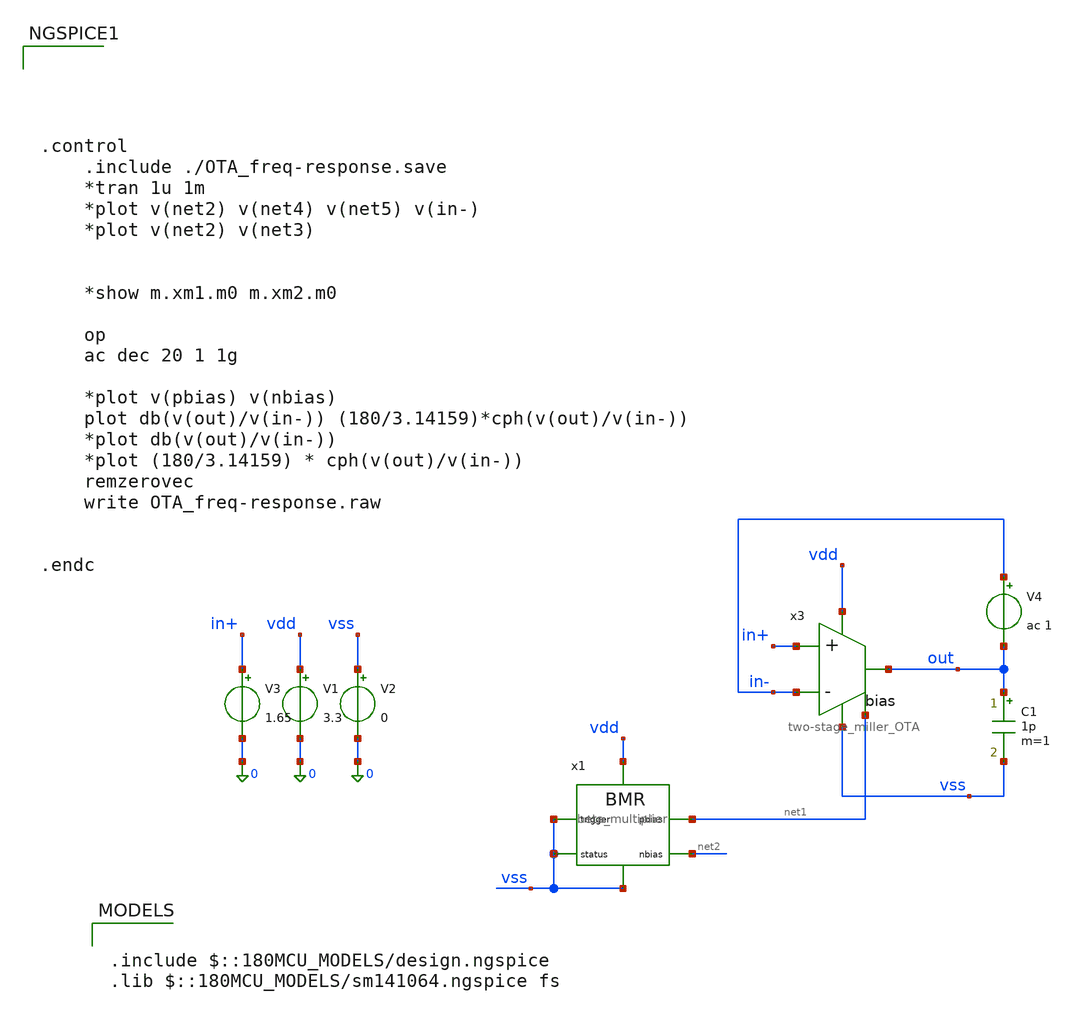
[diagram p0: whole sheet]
** sch_path: simulation/testbench_analog/OTA/OTA_freq-response.sch
**.subckt OTA_freq-response
V3 in+ 0 1.65
V1 vdd 0 3.3
V2 vss 0 0
V4 in- out ac 1
C1 out vss 1p m=1
x3 vdd out in+ in- net1 vss two-stage_miller_OTA
x1 vdd net1 net2 vss vss vss beta_multiplier
**** begin user architecture code





.control
	.include ./OTA_freq-response.save
	*tran 1u 1m
	*plot v(net2) v(net4) v(net5) v(in-)
	*plot v(net2) v(net3)


	*show m.xm1.m0 m.xm2.m0

	op
	ac dec 20 1 1g

	*plot v(pbias) v(nbias)
	plot db(v(out)/v(in-)) (180/3.14159)*cph(v(out)/v(in-))
	*plot db(v(out)/v(in-))
	*plot (180/3.14159) * cph(v(out)/v(in-))
	remzerovec
	write OTA_freq-response.raw


.endc



.include $::180MCU_MODELS/design.ngspice
.lib $::180MCU_MODELS/sm141064.ngspice fs

**** end user architecture code
**.ends

* expanding   symbol:
*+  /foss/designs/acoustic-ranger-dvl-processor/design/analog/OTA/two-stage_miller_OTA.sym # of pins=6
** sym_path: design/analog/OTA/two-stage_miller_OTA.sym
** sch_path: design/analog/OTA/two-stage_miller_OTA.sch
.subckt two-stage_miller_OTA vdd out in+ in- bias vss
*.ipin in+
*.ipin in-
*.opin out
*.iopin vdd
*.iopin vss
*.ipin bias
XM1 net2 in- net1 vdd pfet_03v3 L=1u W=6.2u nf=1 ad='int((nf+1)/2) * W/nf * 0.18u' as='int((nf+2)/2) * W/nf * 0.18u'
+ pd='2*int((nf+1)/2) * (W/nf + 0.18u)' ps='2*int((nf+2)/2) * (W/nf + 0.18u)' nrd='0.18u / W' nrs='0.18u / W'
+ sa=0 sb=0 sd=0 m=8
XM2 net3 in+ net1 vdd pfet_03v3 L=1u W=6.2u nf=1 ad='int((nf+1)/2) * W/nf * 0.18u' as='int((nf+2)/2) * W/nf * 0.18u'
+ pd='2*int((nf+1)/2) * (W/nf + 0.18u)' ps='2*int((nf+2)/2) * (W/nf + 0.18u)' nrd='0.18u / W' nrs='0.18u / W'
+ sa=0 sb=0 sd=0 m=8
XM14 net3 net2 vss vss nfet_03v3 L=3u W=7.7u nf=4 ad='int((nf+1)/2) * W/nf * 0.18u' as='int((nf+2)/2) * W/nf * 0.18u'
+ pd='2*int((nf+1)/2) * (W/nf + 0.18u)' ps='2*int((nf+2)/2) * (W/nf + 0.18u)' nrd='0.18u / W' nrs='0.18u / W'
+ sa=0 sb=0 sd=0 m=2
XM15 net2 net2 vss vss nfet_03v3 L=3u W=7.7u nf=4 ad='int((nf+1)/2) * W/nf * 0.18u' as='int((nf+2)/2) * W/nf * 0.18u'
+ pd='2*int((nf+1)/2) * (W/nf + 0.18u)' ps='2*int((nf+2)/2) * (W/nf + 0.18u)' nrd='0.18u / W' nrs='0.18u / W'
+ sa=0 sb=0 sd=0 m=2
XM3 out net3 vss vss nfet_03v3 L=3u W=7.7u nf=4 ad='int((nf+1)/2) * W/nf * 0.18u' as='int((nf+2)/2) * W/nf * 0.18u'
+ pd='2*int((nf+1)/2) * (W/nf + 0.18u)' ps='2*int((nf+2)/2) * (W/nf + 0.18u)' nrd='0.18u / W' nrs='0.18u / W'
+ sa=0 sb=0 sd=0 m=12
C1 out net3 5p m=1
XM4 net1 bias vdd vdd pfet_03v3 L=20u W=25.3u nf=2 ad='int((nf+1)/2) * W/nf * 0.18u' as='int((nf+2)/2) * W/nf * 0.18u'
+ pd='2*int((nf+1)/2) * (W/nf + 0.18u)' ps='2*int((nf+2)/2) * (W/nf + 0.18u)' nrd='0.18u / W' nrs='0.18u / W'
+ sa=0 sb=0 sd=0 m=2
XM5 out bias vdd vdd pfet_03v3 L=20u W=25.3u nf=2 ad='int((nf+1)/2) * W/nf * 0.18u' as='int((nf+2)/2) * W/nf * 0.18u'
+ pd='2*int((nf+1)/2) * (W/nf + 0.18u)' ps='2*int((nf+2)/2) * (W/nf + 0.18u)' nrd='0.18u / W' nrs='0.18u / W'
+ sa=0 sb=0 sd=0 m=6
.ends


* expanding   symbol:  /foss/designs/acoustic-ranger-dvl-processor/design/analog/beta
*+ multiplier/beta_multiplier.sym # of pins=6
** sym_path: design/analog/beta multiplier/beta_multiplier.sym
** sch_path: design/analog/beta multiplier/beta_multiplier.sch
.subckt beta_multiplier vdd pbias nbias status trigger vss
*.iopin vdd
*.iopin vss
*.opin pbias
*.opin nbias
*.opin status
*.ipin trigger
XM1 pbias nbias net1 net1 nfet_03v3 L=30u W=51.28u nf=1 ad='int((nf+1)/2) * W/nf * 0.18u' as='int((nf+2)/2) * W/nf * 0.18u'
+ pd='2*int((nf+1)/2) * (W/nf + 0.18u)' ps='2*int((nf+2)/2) * (W/nf + 0.18u)' nrd='0.18u / W' nrs='0.18u / W'
+ sa=0 sb=0 sd=0 m=3
XM2 nbias nbias vss vss nfet_03v3 L=30u W=22.22u nf=1 ad='int((nf+1)/2) * W/nf * 0.18u' as='int((nf+2)/2) * W/nf * 0.18u'
+ pd='2*int((nf+1)/2) * (W/nf + 0.18u)' ps='2*int((nf+2)/2) * (W/nf + 0.18u)' nrd='0.18u / W' nrs='0.18u / W'
+ sa=0 sb=0 sd=0 m=3
XM3 pbias pbias vdd vdd pfet_03v3 L=30u W=52.08u nf=1 ad='int((nf+1)/2) * W/nf * 0.18u' as='int((nf+2)/2) * W/nf * 0.18u'
+ pd='2*int((nf+1)/2) * (W/nf + 0.18u)' ps='2*int((nf+2)/2) * (W/nf + 0.18u)' nrd='0.18u / W' nrs='0.18u / W'
+ sa=0 sb=0 sd=0 m=6
XM4 nbias pbias vdd vdd pfet_03v3 L=30u W=52.08u nf=1 ad='int((nf+1)/2) * W/nf * 0.18u' as='int((nf+2)/2) * W/nf * 0.18u'
+ pd='2*int((nf+1)/2) * (W/nf + 0.18u)' ps='2*int((nf+2)/2) * (W/nf + 0.18u)' nrd='0.18u / W' nrs='0.18u / W'
+ sa=0 sb=0 sd=0 m=6
R1 net1 vss 10k m=1
XM5 pbias trigger vss vss nfet_03v3 L=5u W=0.28u nf=1 ad='int((nf+1)/2) * W/nf * 0.18u' as='int((nf+2)/2) * W/nf * 0.18u'
+ pd='2*int((nf+1)/2) * (W/nf + 0.18u)' ps='2*int((nf+2)/2) * (W/nf + 0.18u)' nrd='0.18u / W' nrs='0.18u / W'
+ sa=0 sb=0 sd=0 m=1
XM10 net2 nbias vss vss nfet_03v3 L=0.28u W=18u nf=1 ad='int((nf+1)/2) * W/nf * 0.18u' as='int((nf+2)/2) * W/nf * 0.18u'
+ pd='2*int((nf+1)/2) * (W/nf + 0.18u)' ps='2*int((nf+2)/2) * (W/nf + 0.18u)' nrd='0.18u / W' nrs='0.18u / W'
+ sa=0 sb=0 sd=0 m=1
R3 vdd net2 10k m=1
XM11 status net2 vss vss nfet_03v3 L=1u W=1u nf=1 ad='int((nf+1)/2) * W/nf * 0.18u' as='int((nf+2)/2) * W/nf * 0.18u'
+ pd='2*int((nf+1)/2) * (W/nf + 0.18u)' ps='2*int((nf+2)/2) * (W/nf + 0.18u)' nrd='0.18u / W' nrs='0.18u / W'
+ sa=0 sb=0 sd=0 m=1
XM12 status net2 vdd vdd pfet_03v3 L=1u W=1u nf=1 ad='int((nf+1)/2) * W/nf * 0.18u' as='int((nf+2)/2) * W/nf * 0.18u'
+ pd='2*int((nf+1)/2) * (W/nf + 0.18u)' ps='2*int((nf+2)/2) * (W/nf + 0.18u)' nrd='0.18u / W' nrs='0.18u / W'
+ sa=0 sb=0 sd=0 m=1
.ends

.end
